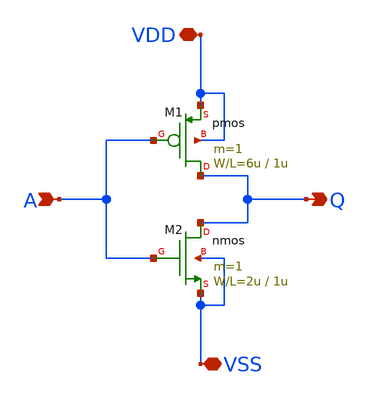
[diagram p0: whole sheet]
** sch_path: member_project/sanken/liuyi/invertar_0614.sch
**.subckt invertar_0614 Q A VDD VSS
*.opin Q
*.ipin A
*.iopin VDD
*.iopin VSS
M1 Q A VDD VDD pmos L=1u W=6u m=1
M2 Q A VSS VSS nmos L=1u W=2u m=1
**.ends
.end
